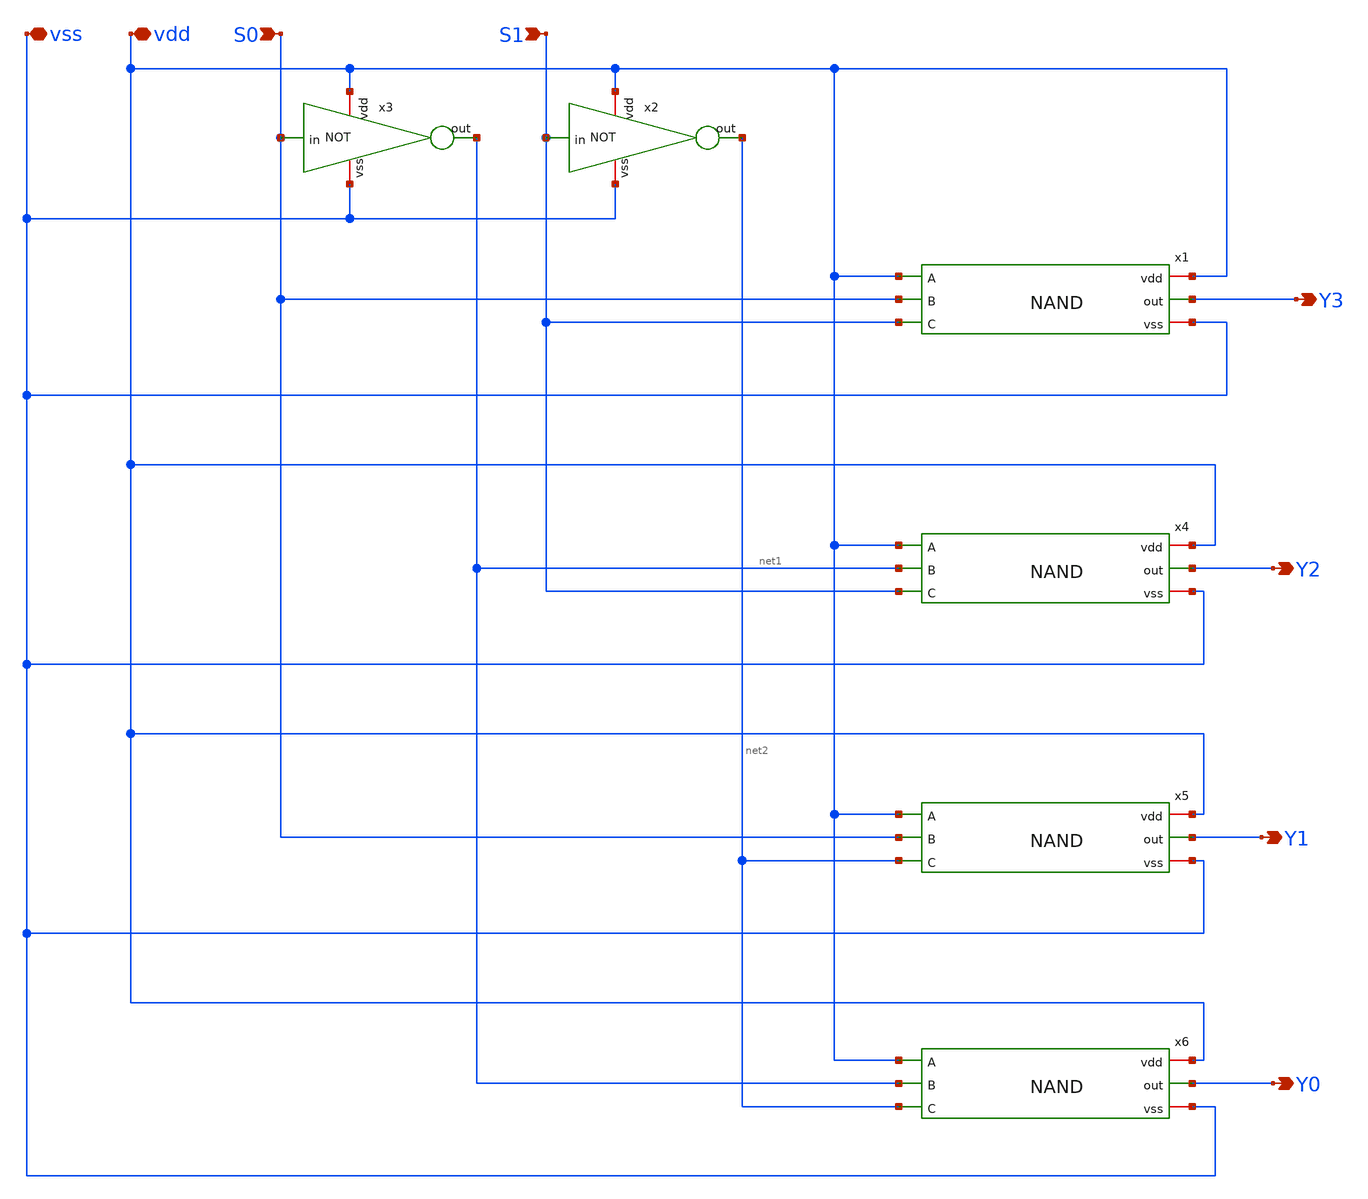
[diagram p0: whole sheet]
** sch_path: BGR_TOP_SKY130A/Dmux1to4_2select_bit.sch
**.subckt Dmux1to4_2select_bit S0 S1 vdd vss Y3 Y2 Y1 Y0
*.ipin S0
*.ipin S1
*.iopin vdd
*.iopin vss
*.opin Y3
*.opin Y2
*.opin Y1
*.opin Y0
x1 vdd Y3 vdd S0 S1 vss NAND
x2 vdd S1 net2 vss NOT
x3 vdd S0 net1 vss NOT
x4 vdd Y2 vdd net1 S1 vss NAND
x5 vdd Y1 vdd S0 net2 vss NAND
x6 vdd Y0 vdd net1 net2 vss NAND
**.ends

* expanding   symbol:  NAND.sym # of pins=6
** sym_path: NAND.sym
** sch_path: NAND.sch
.subckt NAND vdd out A B C vss
*.iopin vdd
*.iopin vss
*.ipin A
*.ipin C
*.ipin B
*.opin out
XM6 out A net1 vss sky130_fd_pr__nfet_01v8_lvt L=1 W=1 nf=1 ad='int((1 + 1)/2) * 1 / 1 * 0.29' as='int((1 + 2)/2) * 1 / 1 * 0.29'
+ pd='2*int((1 + 1)/2) * (1 / 1 + 0.29)' ps='2*int((1 + 2)/2) * (1 / 1 + 0.29)' nrd='0.29 / 1 ' nrs='0.29 / 1 '
+ sa=0 sb=0 sd=0 mult=2 m=2
XM1 out B vdd vdd sky130_fd_pr__pfet_01v8_lvt L=1 W=1 nf=1 ad='int((1 + 1)/2) * 1 / 1 * 0.29' as='int((1 + 2)/2) * 1 / 1 * 0.29'
+ pd='2*int((1 + 1)/2) * (1 / 1 + 0.29)' ps='2*int((1 + 2)/2) * (1 / 1 + 0.29)' nrd='0.29 / 1 ' nrs='0.29 / 1 '
+ sa=0 sb=0 sd=0 mult=4 m=4
XM2 out A vdd vdd sky130_fd_pr__pfet_01v8_lvt L=1 W=1 nf=1 ad='int((1 + 1)/2) * 1 / 1 * 0.29' as='int((1 + 2)/2) * 1 / 1 * 0.29'
+ pd='2*int((1 + 1)/2) * (1 / 1 + 0.29)' ps='2*int((1 + 2)/2) * (1 / 1 + 0.29)' nrd='0.29 / 1 ' nrs='0.29 / 1 '
+ sa=0 sb=0 sd=0 mult=4 m=4
XM3 net1 B net2 vss sky130_fd_pr__nfet_01v8_lvt L=1 W=1 nf=1 ad='int((1 + 1)/2) * 1 / 1 * 0.29' as='int((1 + 2)/2) * 1 / 1 * 0.29'
+ pd='2*int((1 + 1)/2) * (1 / 1 + 0.29)' ps='2*int((1 + 2)/2) * (1 / 1 + 0.29)' nrd='0.29 / 1 ' nrs='0.29 / 1 '
+ sa=0 sb=0 sd=0 mult=2 m=2
XM4 out C vdd vdd sky130_fd_pr__pfet_01v8_lvt L=1 W=1 nf=1 ad='int((1 + 1)/2) * 1 / 1 * 0.29' as='int((1 + 2)/2) * 1 / 1 * 0.29'
+ pd='2*int((1 + 1)/2) * (1 / 1 + 0.29)' ps='2*int((1 + 2)/2) * (1 / 1 + 0.29)' nrd='0.29 / 1 ' nrs='0.29 / 1 '
+ sa=0 sb=0 sd=0 mult=4 m=4
XM5 net2 C vss vss sky130_fd_pr__nfet_01v8_lvt L=1 W=1 nf=1 ad='int((1 + 1)/2) * 1 / 1 * 0.29' as='int((1 + 2)/2) * 1 / 1 * 0.29'
+ pd='2*int((1 + 1)/2) * (1 / 1 + 0.29)' ps='2*int((1 + 2)/2) * (1 / 1 + 0.29)' nrd='0.29 / 1 ' nrs='0.29 / 1 '
+ sa=0 sb=0 sd=0 mult=2 m=2
.ends


* expanding   symbol:  NOT.sym # of pins=4
** sym_path: BGR_TOP_SKY130A/NOT.sym
** sch_path: BGR_TOP_SKY130A/NOT.sch
.subckt NOT vdd in out vss
*.iopin vdd
*.iopin vss
*.ipin in
*.opin out
XM6 out in vss vss sky130_fd_pr__nfet_01v8_lvt L=1 W=1 nf=1 ad='int((1 + 1)/2) * 1 / 1 * 0.29' as='int((1 + 2)/2) * 1 / 1 * 0.29'
+ pd='2*int((1 + 1)/2) * (1 / 1 + 0.29)' ps='2*int((1 + 2)/2) * (1 / 1 + 0.29)' nrd='0.29 / 1 ' nrs='0.29 / 1 '
+ sa=0 sb=0 sd=0 mult=1 m=1
XM1 out in vdd vdd sky130_fd_pr__pfet_01v8_lvt L=1 W=1 nf=1 ad='int((1 + 1)/2) * 1 / 1 * 0.29' as='int((1 + 2)/2) * 1 / 1 * 0.29'
+ pd='2*int((1 + 1)/2) * (1 / 1 + 0.29)' ps='2*int((1 + 2)/2) * (1 / 1 + 0.29)' nrd='0.29 / 1 ' nrs='0.29 / 1 '
+ sa=0 sb=0 sd=0 mult=2 m=2
.ends

.end
